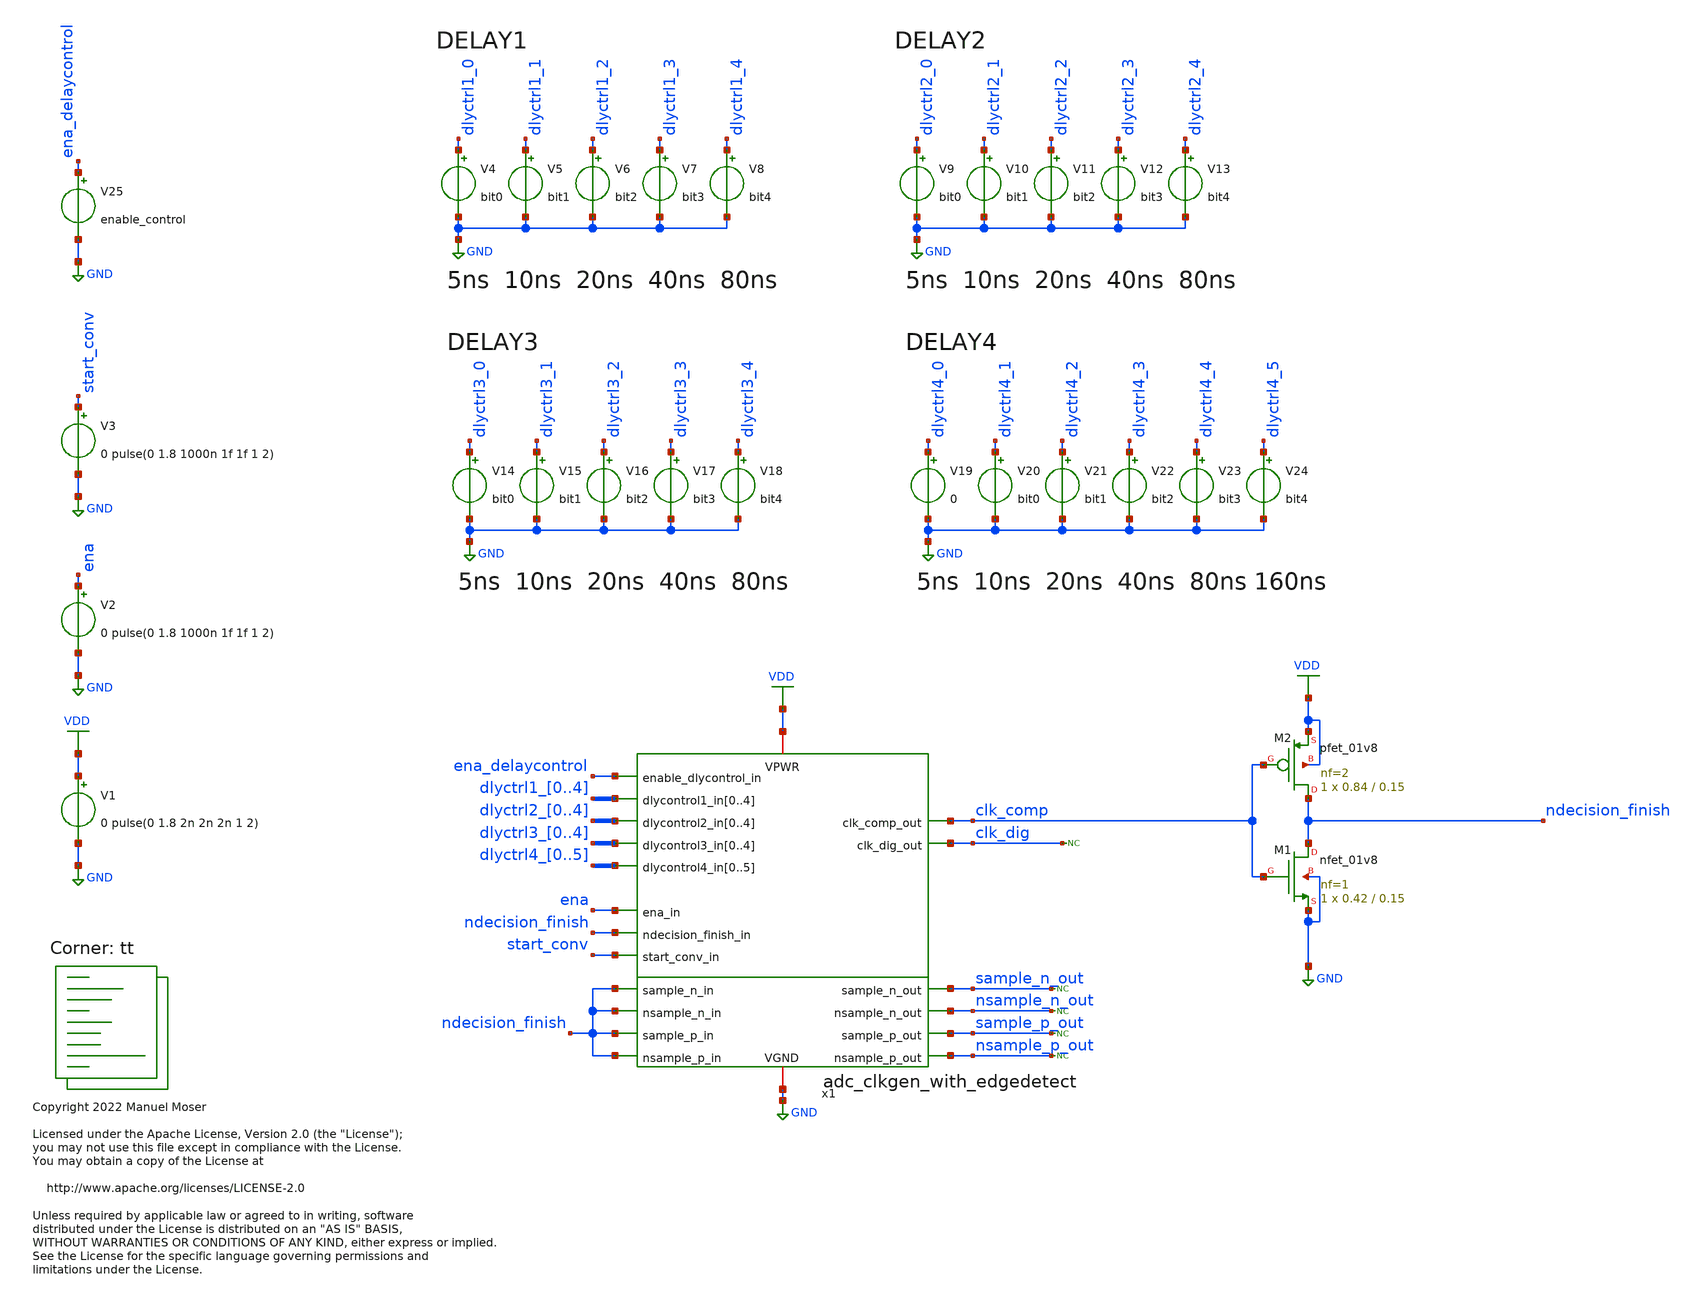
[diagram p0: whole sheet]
** sch_path: openlane/adc_clkgen_with_edgedetect/sim/adc_clkgen_with_edgedetect_tb.sch
* Copyright 2022 Manuel Moser
* Licensed under the Apache License, Version 2.0 (the "License");
**.subckt adc_clkgen_with_edgedetect_tb
x1 GND VDD clk_comp clk_dig dlyctrl1_0 dlyctrl1_1 dlyctrl1_2 dlyctrl1_3 dlyctrl1_4 dlyctrl2_0
+ dlyctrl2_1 dlyctrl2_2 dlyctrl2_3 dlyctrl2_4 dlyctrl3_0 dlyctrl3_1 dlyctrl3_2 dlyctrl3_3 dlyctrl3_4 dlyctrl4_0
+ dlyctrl4_1 dlyctrl4_2 dlyctrl4_3 dlyctrl4_4 dlyctrl4_5 ena ena_delaycontrol ndecision_finish ndecision_finish
+ nsample_n_out ndecision_finish nsample_p_out ndecision_finish sample_n_out ndecision_finish sample_p_out
+ start_conv adc_clkgen_with_edgedetect
V1 VDD GND 0 pulse(0 1.8 2n 2n 2n 1 2)
* noconn clk_dig
* noconn sample_n_out
* noconn nsample_n_out
* noconn sample_p_out
* noconn nsample_p_out
V2 ena GND 0 pulse(0 1.8 1000n 1f 1f 1 2)
V3 start_conv GND 0 pulse(0 1.8 1000n 1f 1f 1 2)
V4 dlyctrl1_0 GND bit0
V5 dlyctrl1_1 GND bit1
V6 dlyctrl1_2 GND bit2
V7 dlyctrl1_3 GND bit3
V8 dlyctrl1_4 GND bit4
V9 dlyctrl2_0 GND bit0
V10 dlyctrl2_1 GND bit1
V11 dlyctrl2_2 GND bit2
V12 dlyctrl2_3 GND bit3
V13 dlyctrl2_4 GND bit4
V14 dlyctrl3_0 GND bit0
V15 dlyctrl3_1 GND bit1
V16 dlyctrl3_2 GND bit2
V17 dlyctrl3_3 GND bit3
V18 dlyctrl3_4 GND bit4
V19 dlyctrl4_0 GND 0
V20 dlyctrl4_1 GND bit0
V21 dlyctrl4_2 GND bit1
V22 dlyctrl4_3 GND bit2
V23 dlyctrl4_4 GND bit3
V24 dlyctrl4_5 GND bit4
V25 ena_delaycontrol GND enable_control
XM2 ndecision_finish clk_comp VDD VDD sky130_fd_pr__pfet_01v8 L=0.15 W=0.84 nf=2 ad='int((nf+1)/2) * W/nf * 0.29'
+ as='int((nf+2)/2) * W/nf * 0.29' pd='2*int((nf+1)/2) * (W/nf + 0.29)' ps='2*int((nf+2)/2) * (W/nf + 0.29)'
+ nrd='0.29 / W' nrs='0.29 / W' sa=0 sb=0 sd=0 mult=1 m=1
XM1 ndecision_finish clk_comp GND GND sky130_fd_pr__nfet_01v8 L=0.15 W=0.42 nf=1 ad='int((nf+1)/2) * W/nf * 0.29'
+ as='int((nf+2)/2) * W/nf * 0.29' pd='2*int((nf+1)/2) * (W/nf + 0.29)' ps='2*int((nf+2)/2) * (W/nf + 0.29)'
+ nrd='0.29 / W' nrs='0.29 / W' sa=0 sb=0 sd=0 mult=1 m=1
**** begin user architecture code


.include /foss/designs/SKY130_SAR-ADC/openlane/adc_clkgen_with_edgedetect/validation/adc_clkgen_with_edgedetect.spice
*.OPTIONS RELTOL=.001 TRTOL=1 ABSTOL=1e-16 CHGTOL=1.0e-16 DEFAD=1.0e-16
.save all
.control
.param enable_control=1.8
.param bit0=1.8
.param bit1=0
.param bit2=0
.param bit3=0
.param bit4=0
tran 100p 1200n
plot v(clk_comp) v(ndecision_finish) v(clk_dig)
.endc

.lib $::SKYWATER_MODELS/sky130.lib.spice tt
**** end user architecture code
**.ends
.GLOBAL GND
.GLOBAL VDD
.end
